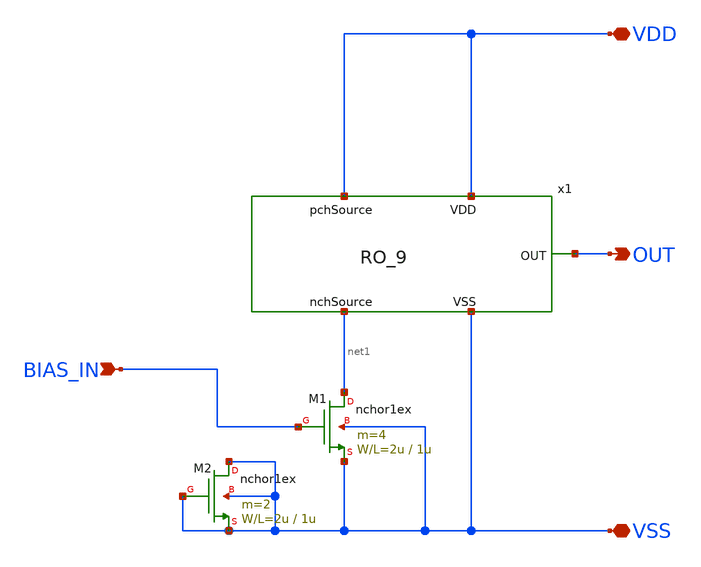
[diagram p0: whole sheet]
** sch_path: design/xschem/VCO/SA_VCO.sch
**.subckt SA_VCO VDD VSS BIAS_IN OUT
*.iopin VDD
*.iopin VSS
*.ipin BIAS_IN
*.opin OUT
x1 VDD VDD VSS net1 OUT RO_9
M1 net1 BIAS_IN VSS VSS nchor1ex L=1u W=2u m=4
M2 VSS VSS VSS VSS nchor1ex L=1u W=2u m=2
**.ends

* expanding   symbol:  VCO/RO_9.sym # of pins=5
** sym_path: design/.design_bk/xschem/VCO/RO_9.sym
** sch_path: design/.design_bk/xschem/VCO/RO_9.sch
.subckt RO_9 pchSource VDD VSS nchSource OUT
*.iopin pchSource
*.iopin VDD
*.iopin VSS
*.iopin nchSource
*.opin OUT
x2 VDD net1 net2 VSS nchSource SA_VCO_INV
x3 VDD net2 net3 VSS nchSource SA_VCO_INV
x4 VDD net3 net4 VSS nchSource SA_VCO_INV
x5 VDD net4 net5 VSS nchSource SA_VCO_INV
x6 VDD net5 net6 VSS nchSource SA_VCO_INV
x7 VDD net6 net7 VSS nchSource SA_VCO_INV
x8 VDD net7 net8 VSS nchSource SA_VCO_INV
x9 VDD net8 net10 VSS nchSource SA_VCO_INV
x10 VDD net8 OUT VSS VSS SA_VCO_INV
x1 VDD net9 net1 VSS nchSource SA_VCO_INV
x11 VDD net10 net11 VSS nchSource SA_VCO_INV
x12 VDD net11 net12 VSS nchSource SA_VCO_INV
x13 VDD net12 net13 VSS nchSource SA_VCO_INV
x14 VDD net13 net14 VSS nchSource SA_VCO_INV
x15 VDD net14 net15 VSS nchSource SA_VCO_INV
x16 VDD net15 net16 VSS nchSource SA_VCO_INV
x17 VDD net16 net17 VSS nchSource SA_VCO_INV
x18 VDD net17 net9 VSS nchSource SA_VCO_INV
.ends


* expanding   symbol:  VCO/SA_VCO_INV.sym # of pins=5
** sym_path: design/xschem/VCO/SA_VCO_INV.sym
** sch_path: design/xschem/VCO/SA_VCO_INV.sch
.subckt SA_VCO_INV VDD IN OUT VSS nchSource
*.iopin nchSource
*.ipin IN
*.opin OUT
*.iopin VDD
*.iopin VSS
M1 VSS OUT VSS VSS nchor1ex L=3u W=6u m=1
M2 OUT IN VDD VDD pchor1ex L=1u W=4u m=4
M3 OUT IN nchSource VSS nchor1ex L=1u W=4u m=2
.ends

.end
